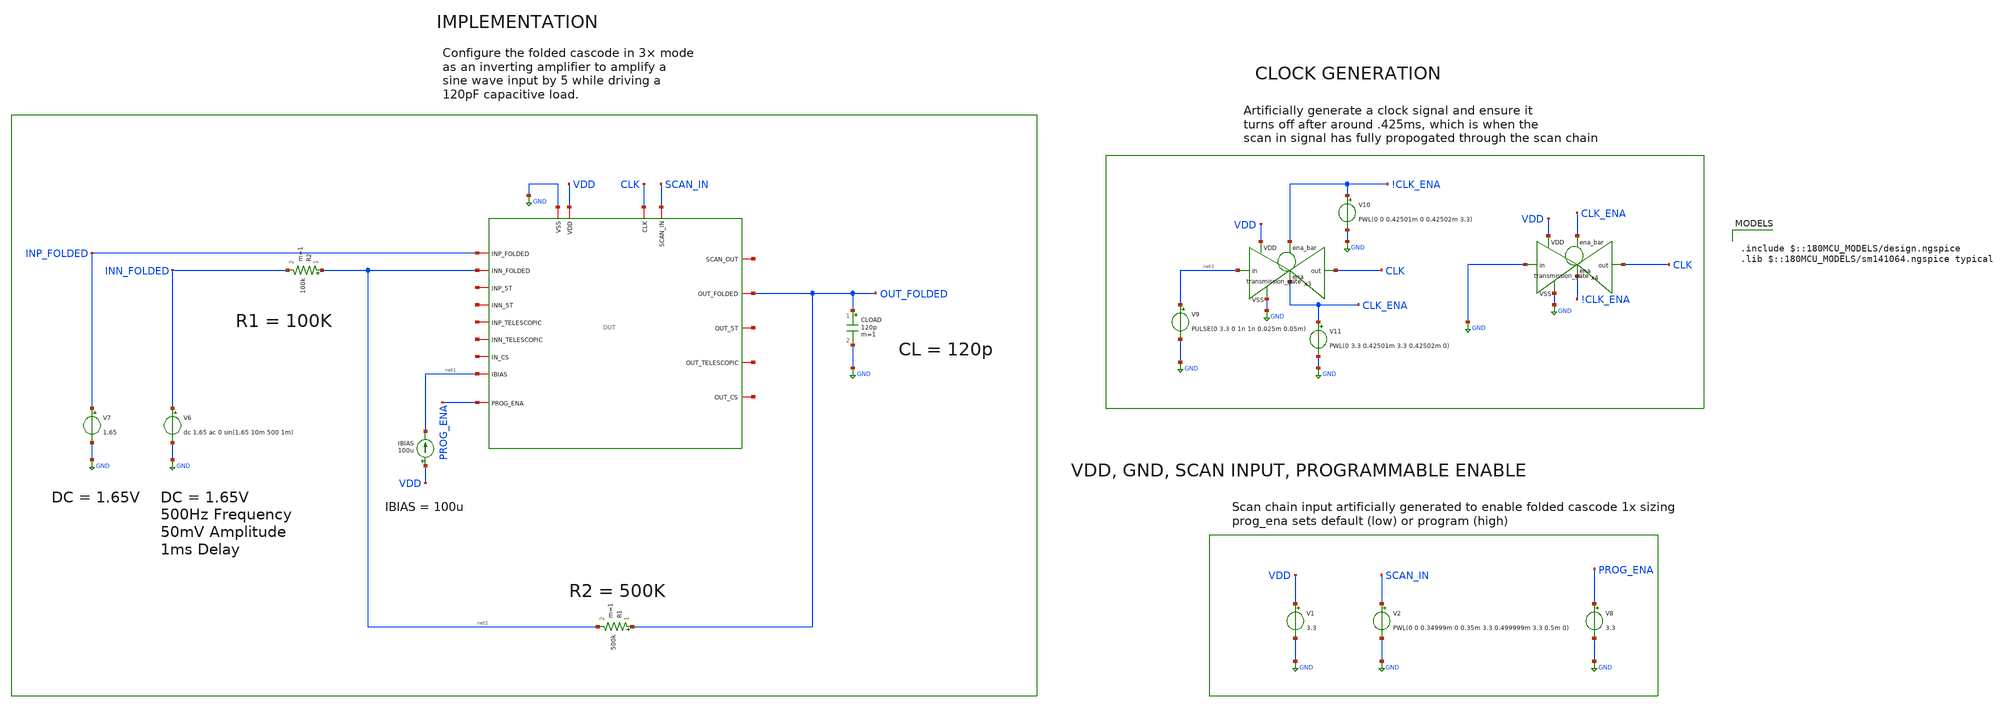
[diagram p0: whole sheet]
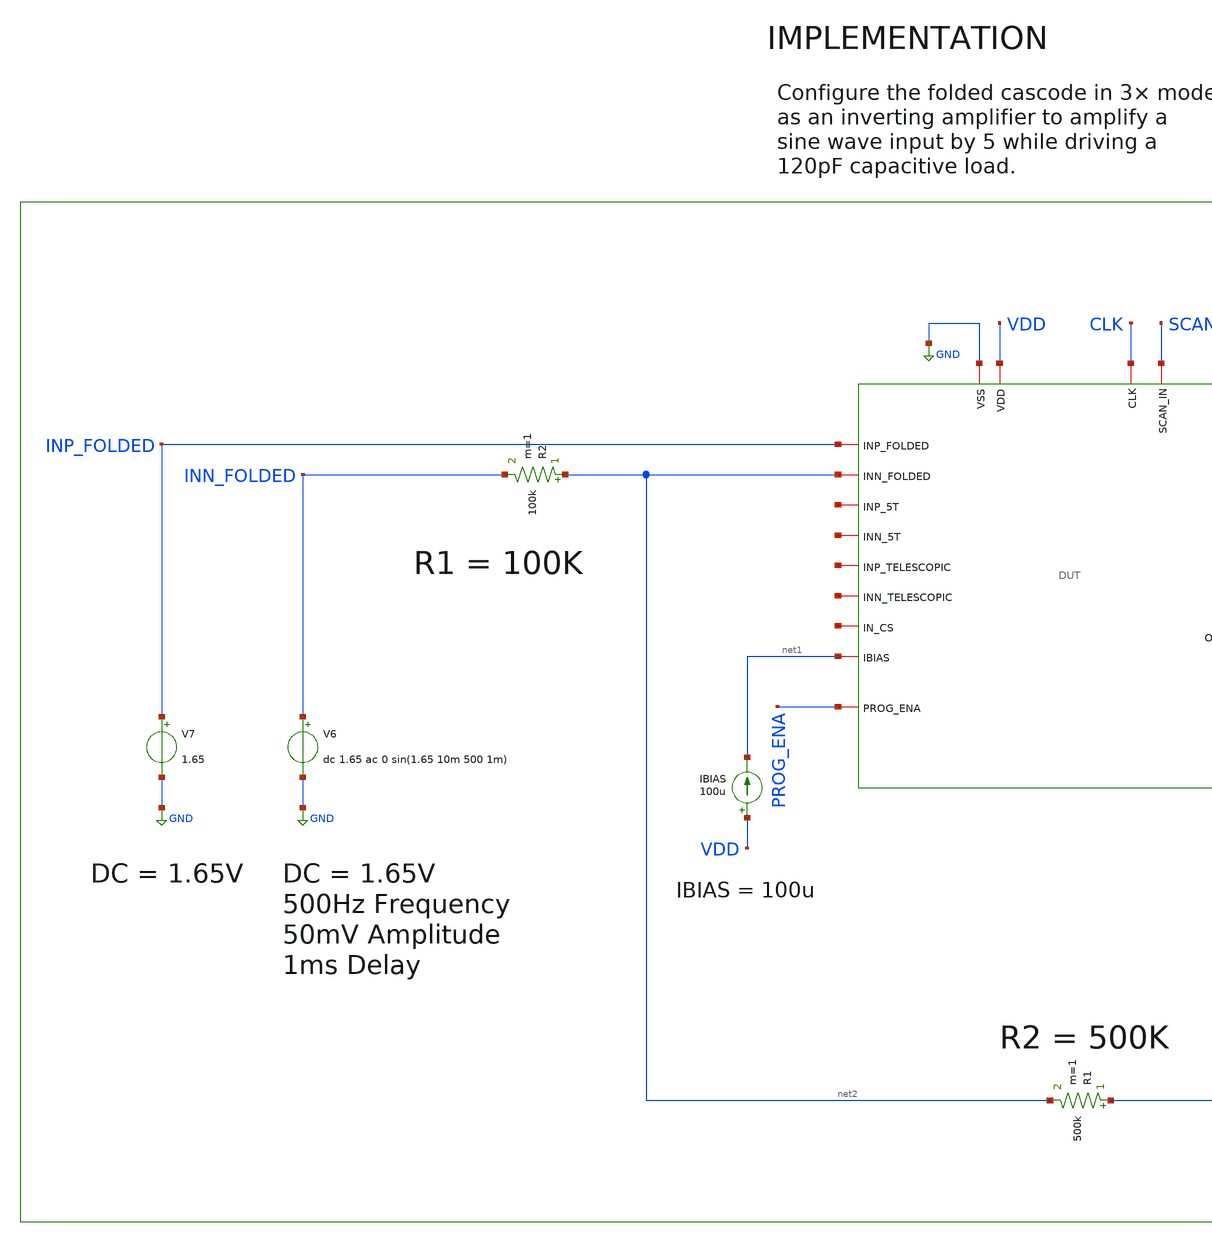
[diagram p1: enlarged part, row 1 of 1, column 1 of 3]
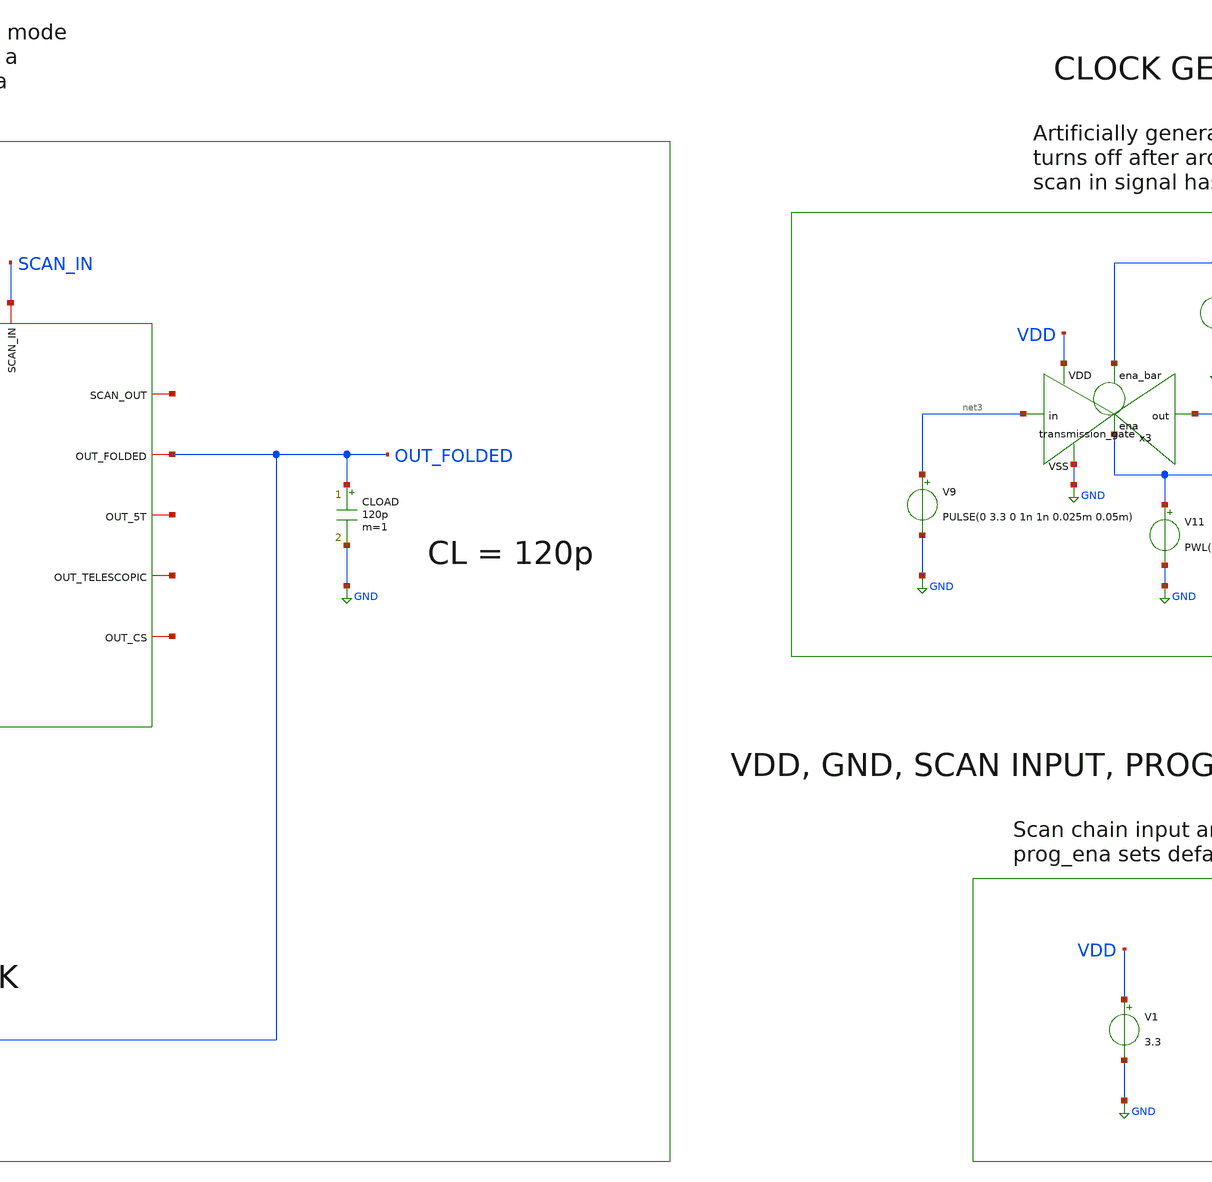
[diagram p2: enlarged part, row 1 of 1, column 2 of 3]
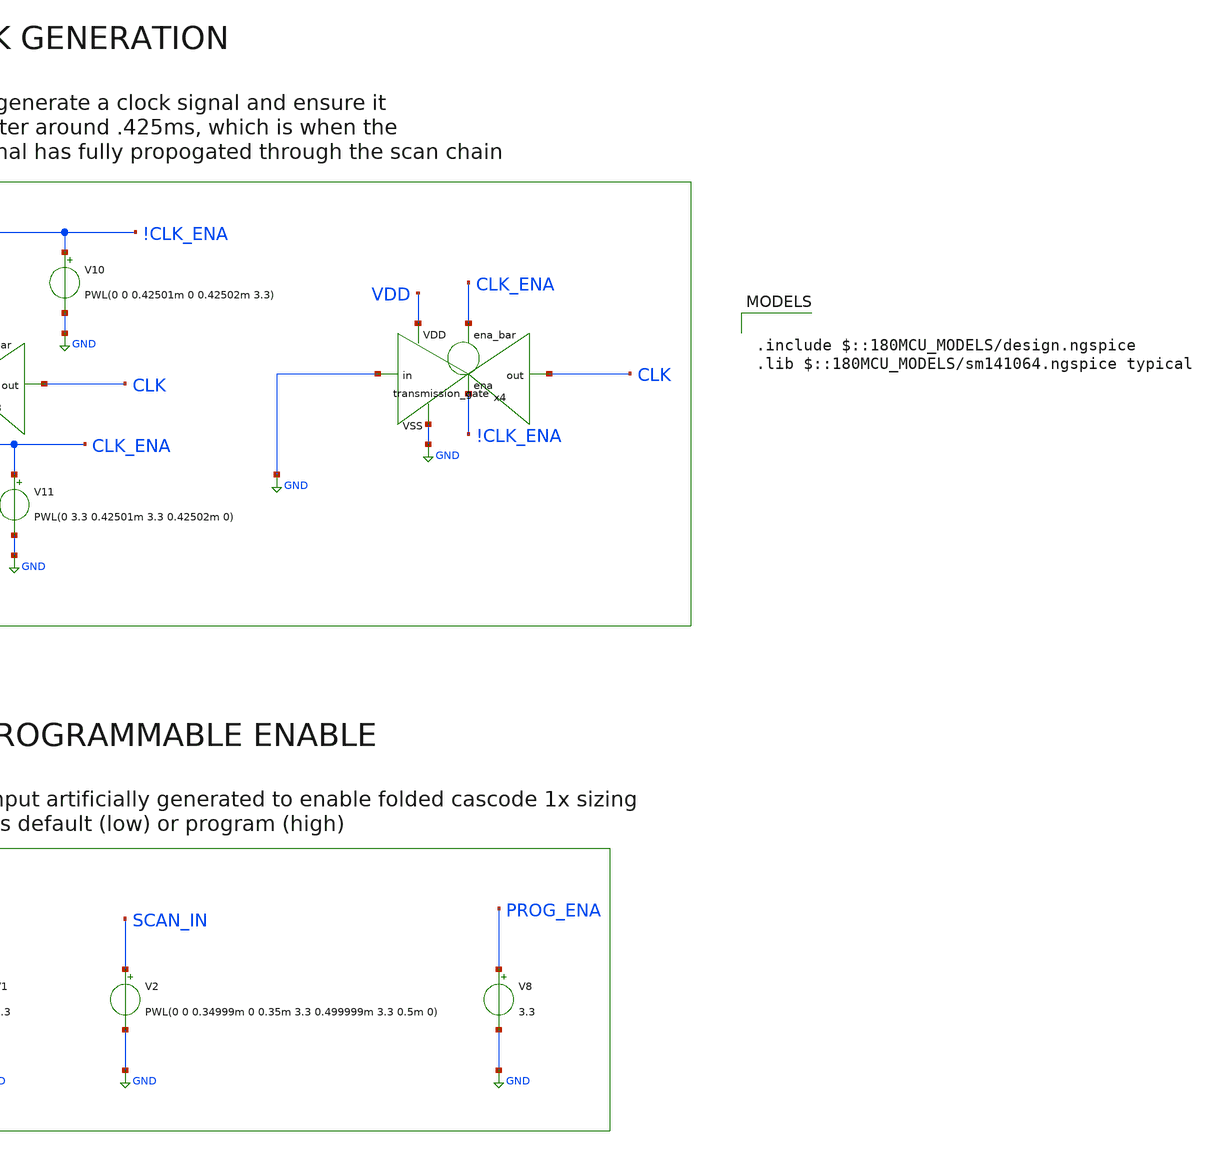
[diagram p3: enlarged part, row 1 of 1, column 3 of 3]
** sch_path: designs/libs/verification/ota_folded/4x_sizing/inverting_amplifier_tb.sch
**.subckt inverting_amplifier_tb
V1 VDD GND 3.3
IBIAS VDD net1 100u
V7 INP_FOLDED GND 1.65
CLOAD OUT_FOLDED GND 120p m=1
R2 net2 INN_FOLDED 100k m=1
V6 INN_FOLDED GND dc 1.65 ac 0 sin(1.65 10m 500 1m)
R1 OUT_FOLDED net2 500k m=1
x1 CLK net4 SCAN_IN GND VDD OUT_FOLDED INP_FOLDED net5 net1 net2 net6 net7 net8 net9 net10 net11
+ net12 PROG_ENA DUT
V8 PROG_ENA GND 3.3
V9 net3 GND PULSE(0 3.3 0 1n 1n 0.025m 0.05m)
x3 !CLK_ENA VDD CLK net3 GND CLK_ENA transmission_gate
V10 !CLK_ENA GND PWL(0 0 0.42501m 0 0.42502m 3.3)
V11 CLK_ENA GND PWL(0 3.3 0.42501m 3.3 0.42502m 0)
x4 CLK_ENA VDD CLK GND GND !CLK_ENA transmission_gate
V2 SCAN_IN GND PWL(0 0 0.34999m 0 0.35m 3.3 0.499999m 3.3 0.5m 0)
**** begin user architecture code

.include $::180MCU_MODELS/design.ngspice
.lib $::180MCU_MODELS/sm141064.ngspice typical



.control
tran 1u 5m

plot v(out_folded) v(inn_folded)

meas tran vout_pp pp v(out_folded) from=2m to=5m
meas tran vin_pp pp v(inn_folded) from=2m to=5m
let gain = vout_pp / vin_pp
print gain

meas tran vout_dc avg v(out_folded) from=2m to=5m
meas tran vin_dc avg v(inn_folded) from=2m to=5m
let dc_offset = vout_dc - vin_dc
let input_offset = dc_offset / 6
print vout_dc vin_dc dc_offset input_offset

let ideal_gain = 5
let gain_error_pct = (ideal_gain - gain) / ideal_gain * 100
print gain_error_pct

meas tran idd avg i(v1) from=2m to=5m
let power = abs(idd) * 3.3
print idd power
.endc


**** end user architecture code
**.ends
.GLOBAL GND
.end
